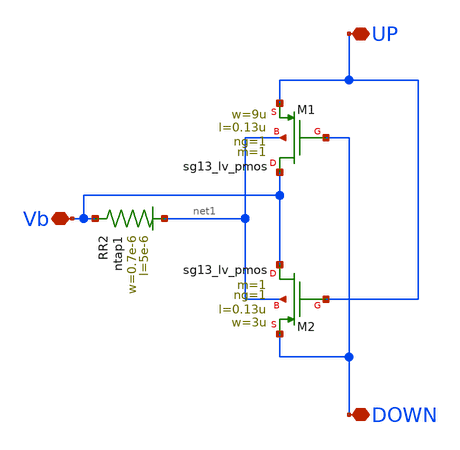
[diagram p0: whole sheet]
** sch_path: Layouts/Body_bias/body_bias.sch
**.subckt body_bias UP DOWN Vb
*.iopin UP
*.iopin DOWN
*.iopin Vb
XM1 Vb DOWN UP net1 sg13_lv_pmos w=9u l=0.13u ng=1 m=1 mm_ok=1
XM2 Vb UP DOWN net1 sg13_lv_pmos w=3u l=0.13u ng=1 m=1 mm_ok=1
XR2 Vb net1 ntap1 R=65.77 w=0.7e-6 l=5e-6
**.ends
.end
